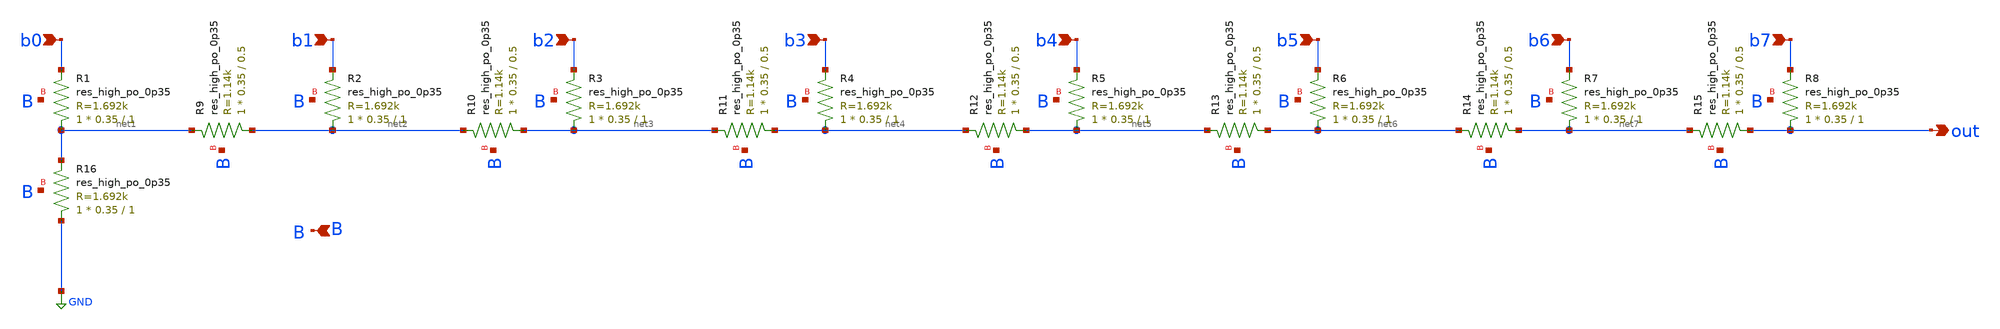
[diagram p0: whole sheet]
** sch_path: xschem/r2r.sch
**.subckt r2r b0 b1 b2 b3 b4 b5 b6 b7 out B
*.ipin b0
*.ipin b1
*.ipin b2
*.ipin b3
*.ipin b4
*.ipin b5
*.ipin b6
*.ipin b7
*.opin out
*.ipin B
XR1 net1 b0 B sky130_fd_pr__res_high_po_0p35 L=1 mult=1 m=1
XR2 net2 b1 B sky130_fd_pr__res_high_po_0p35 L=1 mult=1 m=1
XR3 net3 b2 B sky130_fd_pr__res_high_po_0p35 L=1 mult=1 m=1
XR4 net4 b3 B sky130_fd_pr__res_high_po_0p35 L=1 mult=1 m=1
XR5 net5 b4 B sky130_fd_pr__res_high_po_0p35 L=1 mult=1 m=1
XR6 net6 b5 B sky130_fd_pr__res_high_po_0p35 L=1 mult=1 m=1
XR7 net7 b6 B sky130_fd_pr__res_high_po_0p35 L=1 mult=1 m=1
XR8 out b7 B sky130_fd_pr__res_high_po_0p35 L=1 mult=1 m=1
XR9 net2 net1 B sky130_fd_pr__res_high_po_0p35 L=0.5 mult=1 m=1
XR10 net3 net2 B sky130_fd_pr__res_high_po_0p35 L=0.5 mult=1 m=1
XR11 net4 net3 B sky130_fd_pr__res_high_po_0p35 L=0.5 mult=1 m=1
XR12 net5 net4 B sky130_fd_pr__res_high_po_0p35 L=0.5 mult=1 m=1
XR13 net6 net5 B sky130_fd_pr__res_high_po_0p35 L=0.5 mult=1 m=1
XR14 net7 net6 B sky130_fd_pr__res_high_po_0p35 L=0.5 mult=1 m=1
XR15 out net7 B sky130_fd_pr__res_high_po_0p35 L=0.5 mult=1 m=1
XR16 GND net1 B sky130_fd_pr__res_high_po_0p35 L=1 mult=1 m=1
**.ends
.GLOBAL GND
.end
